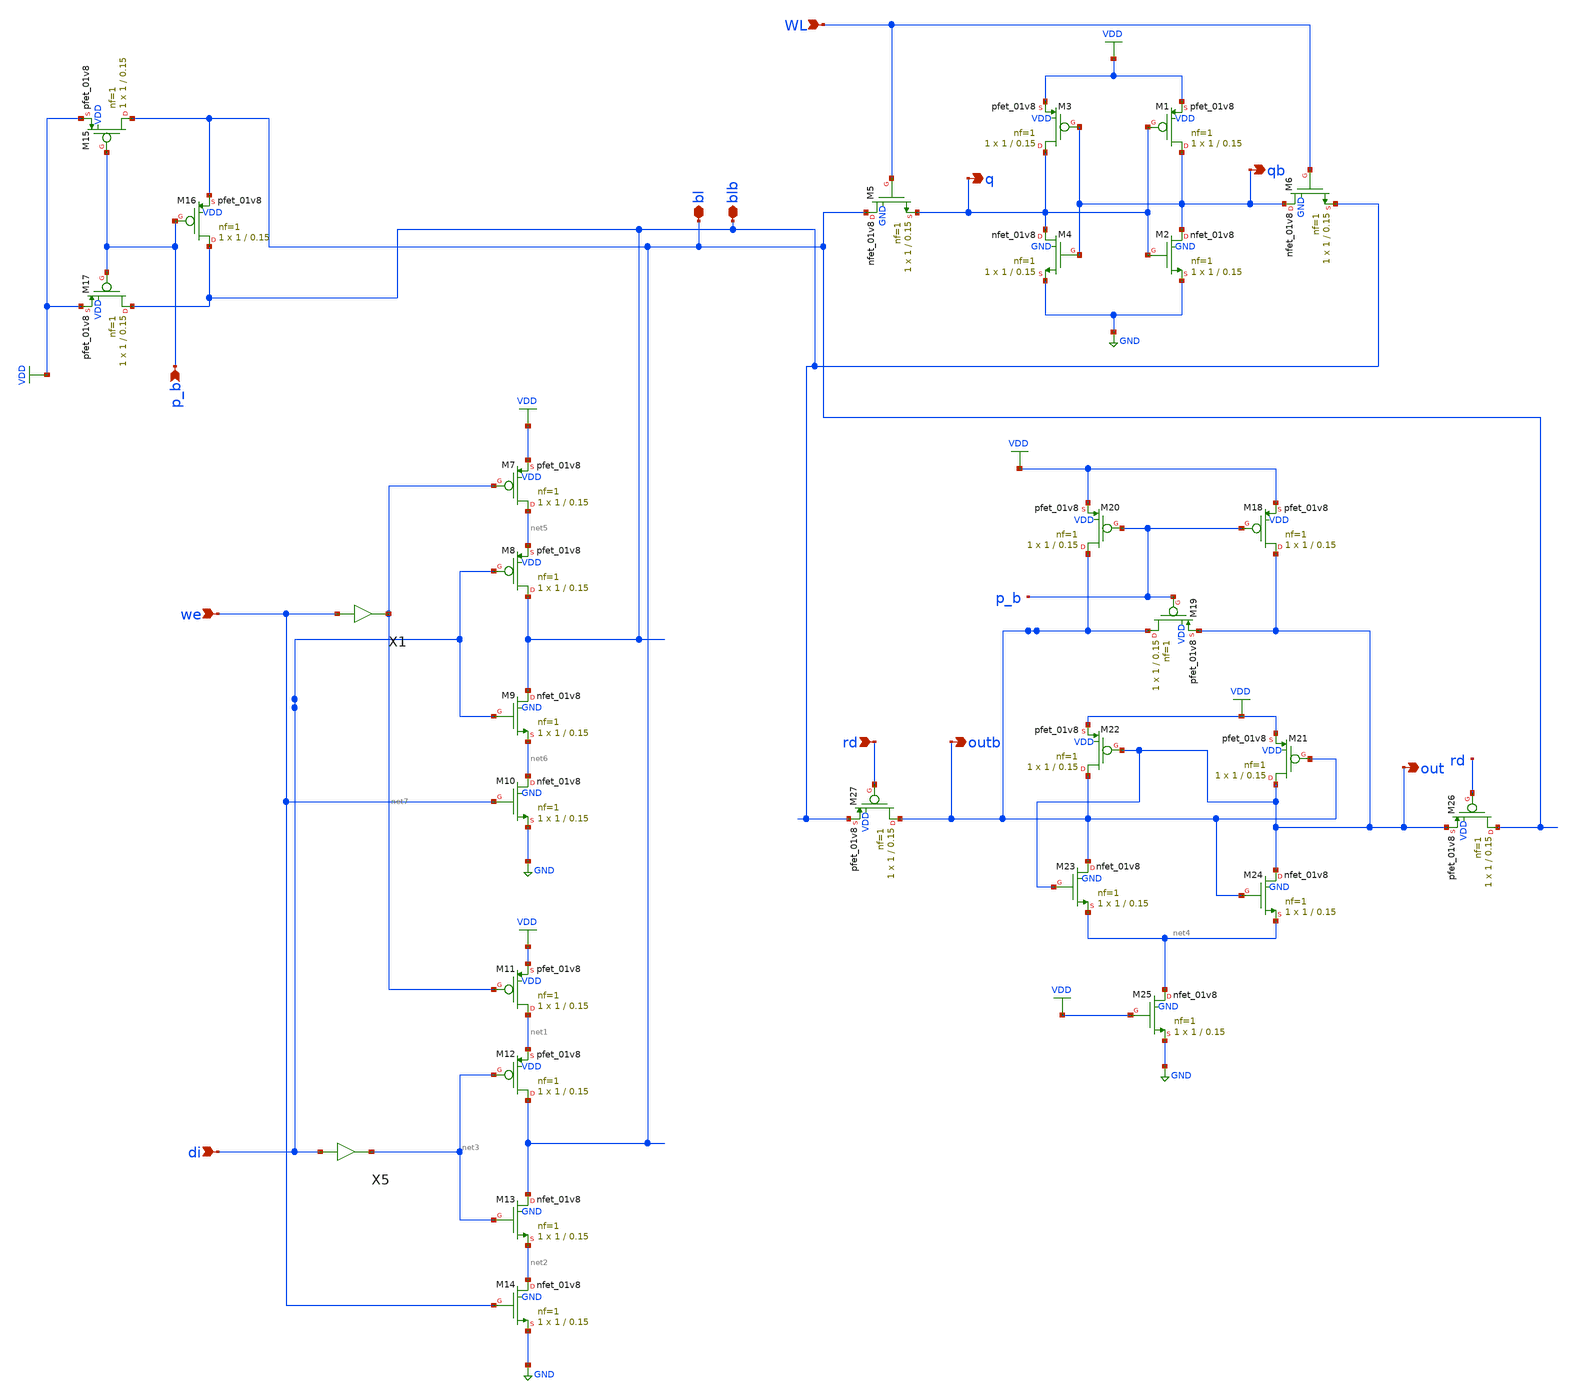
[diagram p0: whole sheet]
** sch_path: gates/Memory/1x1 bit sram.sch
**.subckt 1x1 bit sram WL qb q we di p_b rd out outb blb bl
*.ipin WL
*.opin qb
*.opin q
*.ipin we
*.ipin di
*.ipin p_b
*.ipin rd
*.opin out
*.opin outb
*.iopin blb
*.iopin bl
XM1 qb q VDD VDD sky130_fd_pr__pfet_01v8 L=0.15 W=1 nf=1 ad='int((nf+1)/2) * W/nf * 0.29' as='int((nf+2)/2) * W/nf * 0.29'
+ pd='2*int((nf+1)/2) * (W/nf + 0.29)' ps='2*int((nf+2)/2) * (W/nf + 0.29)' nrd='0.29 / W' nrs='0.29 / W'
+ sa=0 sb=0 sd=0 mult=1 m=1
XM2 qb q GND GND sky130_fd_pr__nfet_01v8 L=0.15 W=1 nf=1 ad='int((nf+1)/2) * W/nf * 0.29' as='int((nf+2)/2) * W/nf * 0.29'
+ pd='2*int((nf+1)/2) * (W/nf + 0.29)' ps='2*int((nf+2)/2) * (W/nf + 0.29)' nrd='0.29 / W' nrs='0.29 / W'
+ sa=0 sb=0 sd=0 mult=1 m=1
XM3 q qb VDD VDD sky130_fd_pr__pfet_01v8 L=0.15 W=1 nf=1 ad='int((nf+1)/2) * W/nf * 0.29' as='int((nf+2)/2) * W/nf * 0.29'
+ pd='2*int((nf+1)/2) * (W/nf + 0.29)' ps='2*int((nf+2)/2) * (W/nf + 0.29)' nrd='0.29 / W' nrs='0.29 / W'
+ sa=0 sb=0 sd=0 mult=1 m=1
XM4 q qb GND GND sky130_fd_pr__nfet_01v8 L=0.15 W=1 nf=1 ad='int((nf+1)/2) * W/nf * 0.29' as='int((nf+2)/2) * W/nf * 0.29'
+ pd='2*int((nf+1)/2) * (W/nf + 0.29)' ps='2*int((nf+2)/2) * (W/nf + 0.29)' nrd='0.29 / W' nrs='0.29 / W'
+ sa=0 sb=0 sd=0 mult=1 m=1
XM5 bl WL q GND sky130_fd_pr__nfet_01v8 L=0.15 W=1 nf=1 ad='int((nf+1)/2) * W/nf * 0.29' as='int((nf+2)/2) * W/nf * 0.29'
+ pd='2*int((nf+1)/2) * (W/nf + 0.29)' ps='2*int((nf+2)/2) * (W/nf + 0.29)' nrd='0.29 / W' nrs='0.29 / W'
+ sa=0 sb=0 sd=0 mult=1 m=1
XM6 qb WL blb GND sky130_fd_pr__nfet_01v8 L=0.15 W=1 nf=1 ad='int((nf+1)/2) * W/nf * 0.29' as='int((nf+2)/2) * W/nf * 0.29'
+ pd='2*int((nf+1)/2) * (W/nf + 0.29)' ps='2*int((nf+2)/2) * (W/nf + 0.29)' nrd='0.29 / W' nrs='0.29 / W'
+ sa=0 sb=0 sd=0 mult=1 m=1
X1 we net7 inv_vtc
X5 di net3 inv_vtc
XM7 net5 net7 VDD VDD sky130_fd_pr__pfet_01v8 L=0.15 W=1 nf=1 ad='int((nf+1)/2) * W/nf * 0.29' as='int((nf+2)/2) * W/nf * 0.29'
+ pd='2*int((nf+1)/2) * (W/nf + 0.29)' ps='2*int((nf+2)/2) * (W/nf + 0.29)' nrd='0.29 / W' nrs='0.29 / W'
+ sa=0 sb=0 sd=0 mult=1 m=1
XM8 blb di net5 VDD sky130_fd_pr__pfet_01v8 L=0.15 W=1 nf=1 ad='int((nf+1)/2) * W/nf * 0.29' as='int((nf+2)/2) * W/nf * 0.29'
+ pd='2*int((nf+1)/2) * (W/nf + 0.29)' ps='2*int((nf+2)/2) * (W/nf + 0.29)' nrd='0.29 / W' nrs='0.29 / W'
+ sa=0 sb=0 sd=0 mult=1 m=1
XM9 blb di net6 GND sky130_fd_pr__nfet_01v8 L=0.15 W=1 nf=1 ad='int((nf+1)/2) * W/nf * 0.29' as='int((nf+2)/2) * W/nf * 0.29'
+ pd='2*int((nf+1)/2) * (W/nf + 0.29)' ps='2*int((nf+2)/2) * (W/nf + 0.29)' nrd='0.29 / W' nrs='0.29 / W'
+ sa=0 sb=0 sd=0 mult=1 m=1
XM10 net6 we GND GND sky130_fd_pr__nfet_01v8 L=0.15 W=1 nf=1 ad='int((nf+1)/2) * W/nf * 0.29' as='int((nf+2)/2) * W/nf * 0.29'
+ pd='2*int((nf+1)/2) * (W/nf + 0.29)' ps='2*int((nf+2)/2) * (W/nf + 0.29)' nrd='0.29 / W' nrs='0.29 / W'
+ sa=0 sb=0 sd=0 mult=1 m=1
XM11 net1 net7 VDD VDD sky130_fd_pr__pfet_01v8 L=0.15 W=1 nf=1 ad='int((nf+1)/2) * W/nf * 0.29' as='int((nf+2)/2) * W/nf * 0.29'
+ pd='2*int((nf+1)/2) * (W/nf + 0.29)' ps='2*int((nf+2)/2) * (W/nf + 0.29)' nrd='0.29 / W' nrs='0.29 / W'
+ sa=0 sb=0 sd=0 mult=1 m=1
XM12 bl net3 net1 VDD sky130_fd_pr__pfet_01v8 L=0.15 W=1 nf=1 ad='int((nf+1)/2) * W/nf * 0.29' as='int((nf+2)/2) * W/nf * 0.29'
+ pd='2*int((nf+1)/2) * (W/nf + 0.29)' ps='2*int((nf+2)/2) * (W/nf + 0.29)' nrd='0.29 / W' nrs='0.29 / W'
+ sa=0 sb=0 sd=0 mult=1 m=1
XM13 bl net3 net2 GND sky130_fd_pr__nfet_01v8 L=0.15 W=1 nf=1 ad='int((nf+1)/2) * W/nf * 0.29' as='int((nf+2)/2) * W/nf * 0.29'
+ pd='2*int((nf+1)/2) * (W/nf + 0.29)' ps='2*int((nf+2)/2) * (W/nf + 0.29)' nrd='0.29 / W' nrs='0.29 / W'
+ sa=0 sb=0 sd=0 mult=1 m=1
XM14 net2 we GND GND sky130_fd_pr__nfet_01v8 L=0.15 W=1 nf=1 ad='int((nf+1)/2) * W/nf * 0.29' as='int((nf+2)/2) * W/nf * 0.29'
+ pd='2*int((nf+1)/2) * (W/nf + 0.29)' ps='2*int((nf+2)/2) * (W/nf + 0.29)' nrd='0.29 / W' nrs='0.29 / W'
+ sa=0 sb=0 sd=0 mult=1 m=1
XM15 bl p_b VDD VDD sky130_fd_pr__pfet_01v8 L=0.15 W=1 nf=1 ad='int((nf+1)/2) * W/nf * 0.29' as='int((nf+2)/2) * W/nf * 0.29'
+ pd='2*int((nf+1)/2) * (W/nf + 0.29)' ps='2*int((nf+2)/2) * (W/nf + 0.29)' nrd='0.29 / W' nrs='0.29 / W'
+ sa=0 sb=0 sd=0 mult=1 m=1
XM16 blb p_b bl VDD sky130_fd_pr__pfet_01v8 L=0.15 W=1 nf=1 ad='int((nf+1)/2) * W/nf * 0.29' as='int((nf+2)/2) * W/nf * 0.29'
+ pd='2*int((nf+1)/2) * (W/nf + 0.29)' ps='2*int((nf+2)/2) * (W/nf + 0.29)' nrd='0.29 / W' nrs='0.29 / W'
+ sa=0 sb=0 sd=0 mult=1 m=1
XM17 blb p_b VDD VDD sky130_fd_pr__pfet_01v8 L=0.15 W=1 nf=1 ad='int((nf+1)/2) * W/nf * 0.29' as='int((nf+2)/2) * W/nf * 0.29'
+ pd='2*int((nf+1)/2) * (W/nf + 0.29)' ps='2*int((nf+2)/2) * (W/nf + 0.29)' nrd='0.29 / W' nrs='0.29 / W'
+ sa=0 sb=0 sd=0 mult=1 m=1
XM18 out p_b VDD VDD sky130_fd_pr__pfet_01v8 L=0.15 W=1 nf=1 ad='int((nf+1)/2) * W/nf * 0.29' as='int((nf+2)/2) * W/nf * 0.29'
+ pd='2*int((nf+1)/2) * (W/nf + 0.29)' ps='2*int((nf+2)/2) * (W/nf + 0.29)' nrd='0.29 / W' nrs='0.29 / W'
+ sa=0 sb=0 sd=0 mult=1 m=1
XM19 outb p_b out VDD sky130_fd_pr__pfet_01v8 L=0.15 W=1 nf=1 ad='int((nf+1)/2) * W/nf * 0.29' as='int((nf+2)/2) * W/nf * 0.29'
+ pd='2*int((nf+1)/2) * (W/nf + 0.29)' ps='2*int((nf+2)/2) * (W/nf + 0.29)' nrd='0.29 / W' nrs='0.29 / W'
+ sa=0 sb=0 sd=0 mult=1 m=1
XM20 outb p_b VDD VDD sky130_fd_pr__pfet_01v8 L=0.15 W=1 nf=1 ad='int((nf+1)/2) * W/nf * 0.29' as='int((nf+2)/2) * W/nf * 0.29'
+ pd='2*int((nf+1)/2) * (W/nf + 0.29)' ps='2*int((nf+2)/2) * (W/nf + 0.29)' nrd='0.29 / W' nrs='0.29 / W'
+ sa=0 sb=0 sd=0 mult=1 m=1
XM21 out outb VDD VDD sky130_fd_pr__pfet_01v8 L=0.15 W=1 nf=1 ad='int((nf+1)/2) * W/nf * 0.29' as='int((nf+2)/2) * W/nf * 0.29'
+ pd='2*int((nf+1)/2) * (W/nf + 0.29)' ps='2*int((nf+2)/2) * (W/nf + 0.29)' nrd='0.29 / W' nrs='0.29 / W'
+ sa=0 sb=0 sd=0 mult=1 m=1
XM22 outb out VDD VDD sky130_fd_pr__pfet_01v8 L=0.15 W=1 nf=1 ad='int((nf+1)/2) * W/nf * 0.29' as='int((nf+2)/2) * W/nf * 0.29'
+ pd='2*int((nf+1)/2) * (W/nf + 0.29)' ps='2*int((nf+2)/2) * (W/nf + 0.29)' nrd='0.29 / W' nrs='0.29 / W'
+ sa=0 sb=0 sd=0 mult=1 m=1
XM23 outb out net4 GND sky130_fd_pr__nfet_01v8 L=0.15 W=1 nf=1 ad='int((nf+1)/2) * W/nf * 0.29' as='int((nf+2)/2) * W/nf * 0.29'
+ pd='2*int((nf+1)/2) * (W/nf + 0.29)' ps='2*int((nf+2)/2) * (W/nf + 0.29)' nrd='0.29 / W' nrs='0.29 / W'
+ sa=0 sb=0 sd=0 mult=1 m=1
XM24 out outb net4 GND sky130_fd_pr__nfet_01v8 L=0.15 W=1 nf=1 ad='int((nf+1)/2) * W/nf * 0.29' as='int((nf+2)/2) * W/nf * 0.29'
+ pd='2*int((nf+1)/2) * (W/nf + 0.29)' ps='2*int((nf+2)/2) * (W/nf + 0.29)' nrd='0.29 / W' nrs='0.29 / W'
+ sa=0 sb=0 sd=0 mult=1 m=1
XM25 net4 VDD GND GND sky130_fd_pr__nfet_01v8 L=0.15 W=1 nf=1 ad='int((nf+1)/2) * W/nf * 0.29' as='int((nf+2)/2) * W/nf * 0.29'
+ pd='2*int((nf+1)/2) * (W/nf + 0.29)' ps='2*int((nf+2)/2) * (W/nf + 0.29)' nrd='0.29 / W' nrs='0.29 / W'
+ sa=0 sb=0 sd=0 mult=1 m=1
XM26 bl rd out VDD sky130_fd_pr__pfet_01v8 L=0.15 W=1 nf=1 ad='int((nf+1)/2) * W/nf * 0.29' as='int((nf+2)/2) * W/nf * 0.29'
+ pd='2*int((nf+1)/2) * (W/nf + 0.29)' ps='2*int((nf+2)/2) * (W/nf + 0.29)' nrd='0.29 / W' nrs='0.29 / W'
+ sa=0 sb=0 sd=0 mult=1 m=1
XM27 outb rd blb VDD sky130_fd_pr__pfet_01v8 L=0.15 W=1 nf=1 ad='int((nf+1)/2) * W/nf * 0.29' as='int((nf+2)/2) * W/nf * 0.29'
+ pd='2*int((nf+1)/2) * (W/nf + 0.29)' ps='2*int((nf+2)/2) * (W/nf + 0.29)' nrd='0.29 / W' nrs='0.29 / W'
+ sa=0 sb=0 sd=0 mult=1 m=1
**.ends

* expanding   symbol:  /home/apn/test_xschem_sky130/inv_vtc.sym # of pins=2
** sym_path: gates/Memory/inv_vtc.sym
** sch_path: gates/Memory/inv_vtc.sch
.subckt inv_vtc A Y
*.ipin A
*.opin Y
XM1 Y A VDD VDD sky130_fd_pr__pfet_01v8 L=0.15 W=2 nf=1 ad='int((nf+1)/2) * W/nf * 0.29' as='int((nf+2)/2) * W/nf * 0.29'
+ pd='2*int((nf+1)/2) * (W/nf + 0.29)' ps='2*int((nf+2)/2) * (W/nf + 0.29)' nrd='0.29 / W' nrs='0.29 / W'
+ sa=0 sb=0 sd=0 mult=1 m=1
XM2 Y A GND GND sky130_fd_pr__nfet_01v8 L=0.15 W=1 nf=1 ad='int((nf+1)/2) * W/nf * 0.29' as='int((nf+2)/2) * W/nf * 0.29'
+ pd='2*int((nf+1)/2) * (W/nf + 0.29)' ps='2*int((nf+2)/2) * (W/nf + 0.29)' nrd='0.29 / W' nrs='0.29 / W'
+ sa=0 sb=0 sd=0 mult=1 m=1
.ends

.GLOBAL GND
.GLOBAL VDD
.end
